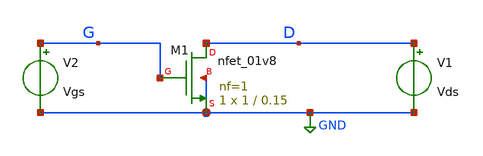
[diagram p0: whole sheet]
** sch_path: sky130A/xschem_libs/sky130_tests/test_nfet_final/schematic/test_nfet_final.sch
**.subckt test_nfet_final
XM1 D G GND GND sky130_fd_pr__nfet_01v8 L=0.15 W=1 nf=1 ad='int((1 + 1)/2) * 1 / 1 * 0.29' as='int((1 + 2)/2) * 1 / 1 * 0.29'
+ pd='2*int((1 + 1)/2) * (1 / 1 + 0.29)' ps='2*int((1 + 2)/2) * (1 / 1 + 0.29)' nrd='0.29 / 1 ' nrs='0.29 / 1 '
+ sa=0 sb=0 sd=0 mult=1 m=1
V1 D GND Vds
V2 G GND Vgs
**.ends
.GLOBAL GND
.end
